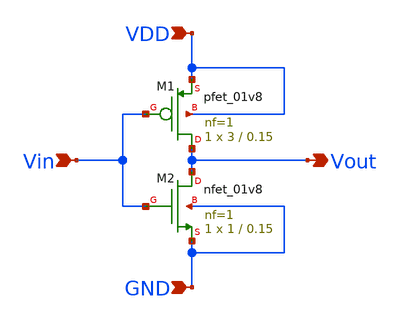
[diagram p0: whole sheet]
** sch_path: CMOS-Inverter-pre-layout-Design-and-Analysis/Inverter.sch
**.subckt Inverter Vin Vout VDD GND
*.ipin Vin
*.opin Vout
*.ipin VDD
*.ipin GND
XM1 Vout Vin VDD VDD sky130_fd_pr__pfet_01v8 L=0.15 W=3 nf=1 ad='int((nf+1)/2) * W/nf * 0.29' as='int((nf+2)/2) * W/nf * 0.29'
+ pd='2*int((nf+1)/2) * (W/nf + 0.29)' ps='2*int((nf+2)/2) * (W/nf + 0.29)' nrd='0.29 / W' nrs='0.29 / W'
+ sa=0 sb=0 sd=0 mult=1 m=1
XM2 Vout Vin GND GND sky130_fd_pr__nfet_01v8 L=0.15 W=1 nf=1 ad='int((nf+1)/2) * W/nf * 0.29' as='int((nf+2)/2) * W/nf * 0.29'
+ pd='2*int((nf+1)/2) * (W/nf + 0.29)' ps='2*int((nf+2)/2) * (W/nf + 0.29)' nrd='0.29 / W' nrs='0.29 / W'
+ sa=0 sb=0 sd=0 mult=1 m=1
**.ends
.end
